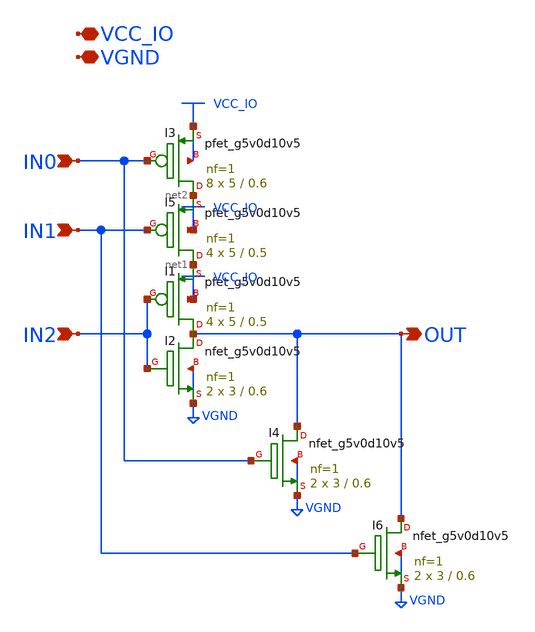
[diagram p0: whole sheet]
** sch_path: com_cclat_hvnor3.sch
* Copyright 2023 David Mitchell Bailey
* Licensed under the Apache License, Version 2.0 (the "License");
* you may not use this file except in compliance with the License.
* You may obtain a copy of the License at
* https://www.apache.org/licenses/LICENSE-2.0
* Unless required by applicable law or agreed to in writing, software
* distributed under the License is distributed on an "AS IS" BASIS,
* WITHOUT WARRANTIES OR CONDITIONS OF ANY KIND, either express or implied.
* See the License for the specific language governing permissions and
* limitations under the License.
**.subckt com_cclat_hvnor3 IN2 OUT VCC_IO VGND IN0 IN1
*.ipin IN2
*.opin OUT
*.iopin VCC_IO
*.iopin VGND
*.ipin IN0
*.ipin IN1
XI2 OUT IN2 VGND VGND sky130_fd_pr__nfet_g5v0d10v5 L=0.6 W=3 nf=1 ad='int((nf+1)/2) * W/nf * 0.29' as='int((nf+2)/2) * W/nf * 0.29'
+ pd='2*int((nf+1)/2) * (W/nf + 0.29)' ps='2*int((nf+2)/2) * (W/nf + 0.29)' nrd='0.29 / W' nrs='0.29 / W'
+ sa=0 sb=0 sd=0 mult=2 m=2
XI1 OUT IN2 net1 VCC_IO sky130_fd_pr__pfet_g5v0d10v5 L=0.5 W=5 nf=1 ad='int((nf+1)/2) * W/nf * 0.29'
+ as='int((nf+2)/2) * W/nf * 0.29' pd='2*int((nf+1)/2) * (W/nf + 0.29)' ps='2*int((nf+2)/2) * (W/nf + 0.29)'
+ nrd='0.29 / W' nrs='0.29 / W' sa=0 sb=0 sd=0 mult=4 m=4
XI3 net2 IN0 VCC_IO VCC_IO sky130_fd_pr__pfet_g5v0d10v5 L=0.6 W=5 nf=1 ad='int((nf+1)/2) * W/nf * 0.29'
+ as='int((nf+2)/2) * W/nf * 0.29' pd='2*int((nf+1)/2) * (W/nf + 0.29)' ps='2*int((nf+2)/2) * (W/nf + 0.29)'
+ nrd='0.29 / W' nrs='0.29 / W' sa=0 sb=0 sd=0 mult=8 m=8
XI4 OUT IN0 VGND VGND sky130_fd_pr__nfet_g5v0d10v5 L=0.6 W=3 nf=1 ad='int((nf+1)/2) * W/nf * 0.29' as='int((nf+2)/2) * W/nf * 0.29'
+ pd='2*int((nf+1)/2) * (W/nf + 0.29)' ps='2*int((nf+2)/2) * (W/nf + 0.29)' nrd='0.29 / W' nrs='0.29 / W'
+ sa=0 sb=0 sd=0 mult=2 m=2
XI5 net1 IN1 net2 VCC_IO sky130_fd_pr__pfet_g5v0d10v5 L=0.5 W=5 nf=1 ad='int((nf+1)/2) * W/nf * 0.29'
+ as='int((nf+2)/2) * W/nf * 0.29' pd='2*int((nf+1)/2) * (W/nf + 0.29)' ps='2*int((nf+2)/2) * (W/nf + 0.29)'
+ nrd='0.29 / W' nrs='0.29 / W' sa=0 sb=0 sd=0 mult=4 m=4
XI6 OUT IN1 VGND VGND sky130_fd_pr__nfet_g5v0d10v5 L=0.6 W=3 nf=1 ad='int((nf+1)/2) * W/nf * 0.29' as='int((nf+2)/2) * W/nf * 0.29'
+ pd='2*int((nf+1)/2) * (W/nf + 0.29)' ps='2*int((nf+2)/2) * (W/nf + 0.29)' nrd='0.29 / W' nrs='0.29 / W'
+ sa=0 sb=0 sd=0 mult=2 m=2
**.ends
.end
